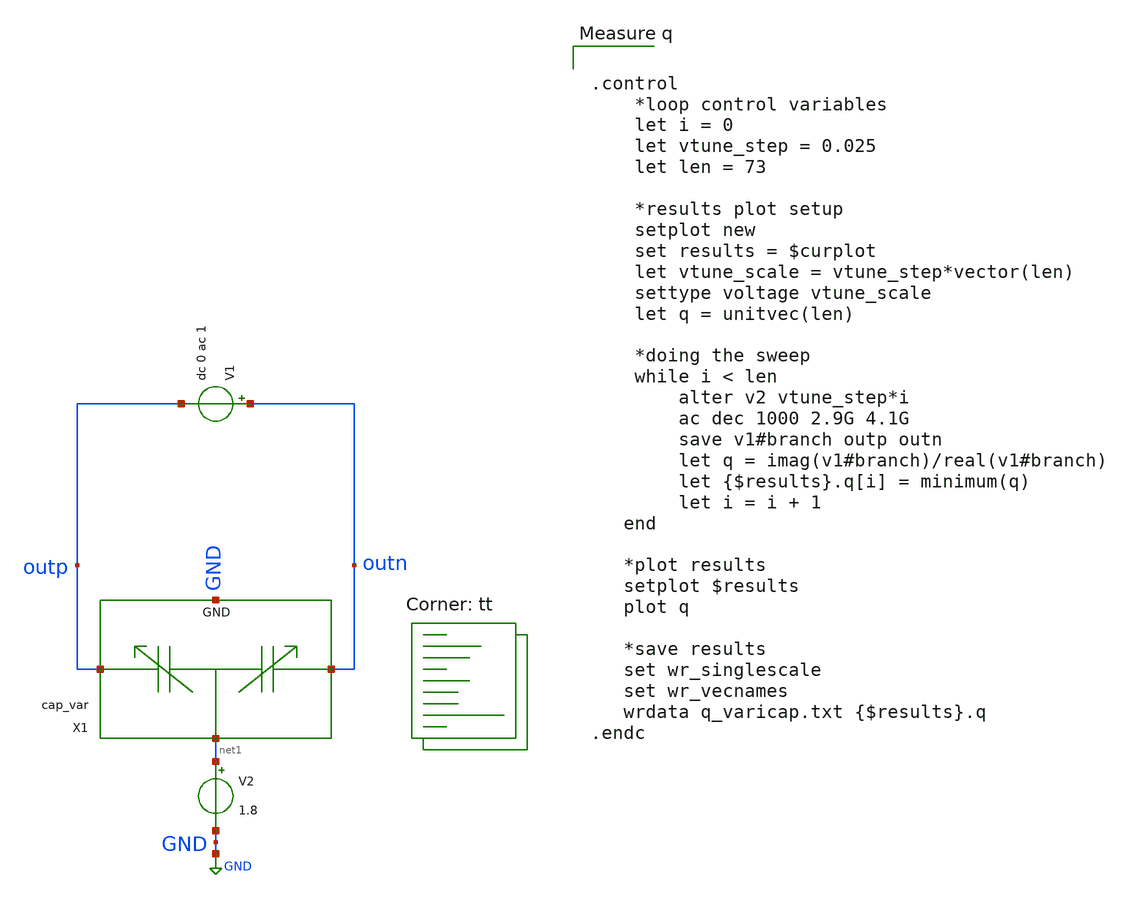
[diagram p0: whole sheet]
** sch_path: xschem/vco/testbenches/varicap/varicap_Q_measurement_tb.sch
**.subckt varicap_Q_measurement_tb
X1 outn outp GND net1 cap_var
V1 outn outp dc 0 ac 1
V2 net1 GND 1.8
**** begin user architecture code
.lib $::SKYWATER_MODELS/sky130.lib.spice tt


.control
    *loop control variables
    let i = 0
    let vtune_step = 0.025
    let len = 73

    *results plot setup
    setplot new
    set results = $curplot
    let vtune_scale = vtune_step*vector(len)
    settype voltage vtune_scale
    let q = unitvec(len)

    *doing the sweep
    while i < len
        alter v2 vtune_step*i
        ac dec 1000 2.9G 4.1G
        save v1#branch outp outn
        let q = imag(v1#branch)/real(v1#branch)
        let {$results}.q[i] = minimum(q)
        let i = i + 1
   end

   *plot results
   setplot $results
   plot q

   *save results
   set wr_singlescale
   set wr_vecnames
   wrdata q_varicap.txt {$results}.q
.endc


**** end user architecture code
**.ends

* expanding   symbol:  vco/parts/cap_var.sym # of pins=4
** sym_path: xschem/vco/parts/cap_var.sym
** sch_path: xschem/vco/parts/cap_var.sch
.subckt cap_var OUT_P OUT_N GND Vtune
*.iopin OUT_P
*.iopin OUT_N
*.iopin GND
*.ipin Vtune
XC1 OUT_P Vtune GND sky130_fd_pr__cap_var_lvt W=4 L=0.6 VM=14 m=14
XC2 OUT_N Vtune GND sky130_fd_pr__cap_var_lvt W=4 L=0.6 VM=14 m=14
.ends

.GLOBAL GND
.end
